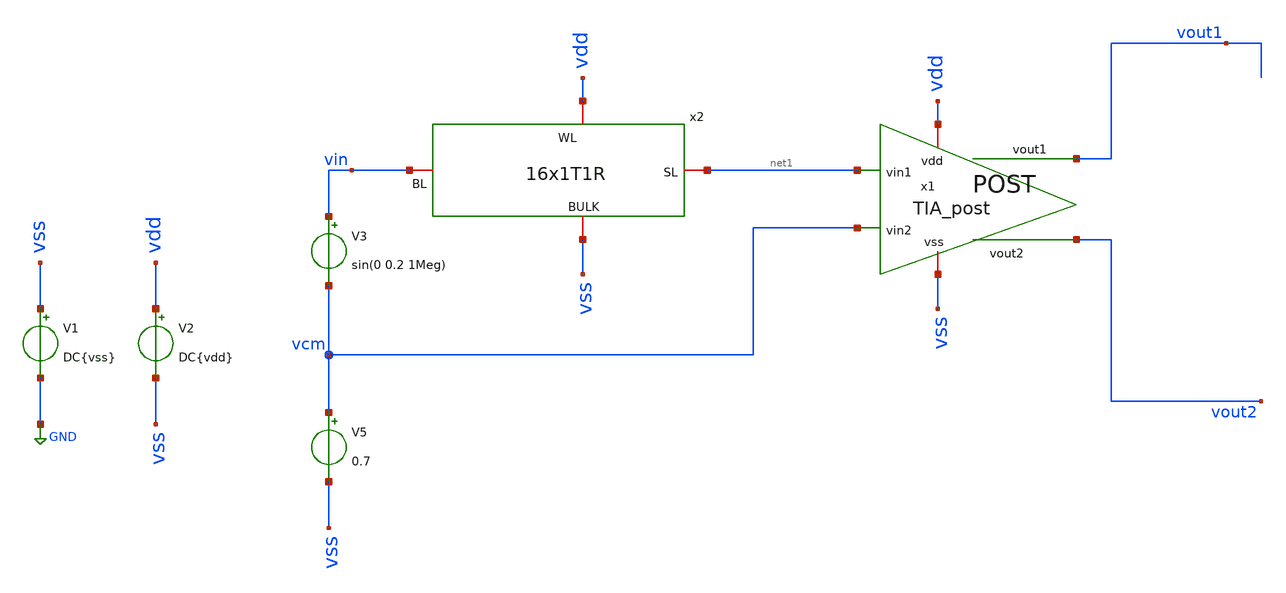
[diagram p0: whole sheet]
** sch_path: sch/tb_full.sch
**.subckt tb_full
V1 vss GND DC{vss}
V2 vdd vss DC{vdd}
V5 vcm vss 0.7
x1 net1 vcm vout1 vout2 vdd vss TIA_post
x2 vdd vin vss net1 16x1T1R
V3 vin vcm sin(0 0.2 1Meg)
.save i(v3)
**** begin user architecture code




* Circuit Parameters
.param iref = 100u
.param vdd  = 1.8
.param vss  = 0.0
.options TEMP = 65.0
.option savecurrents



* OP Parameters & Singals to save
.save all

*Simulations
.control

  reset
  tran 0.01u 2u
  setplot tran1
  plot v(vin) v(vcm) v(vout1) v(vout2)
  plot i(v4)

  write tb_full.raw




.endc

.end



** opencircuitdesign pdks install
.lib $::SKYWATER_MODELS/sky130.lib.spice tt
.inc $::SKYWATER_MODELS/sky130_smooth.spice
* Include Models
.inc /home/alex/Desktop/EDA/TIA_IPN/sch/TIA_post.spice

**** end user architecture code
**.ends
.GLOBAL GND
.end
